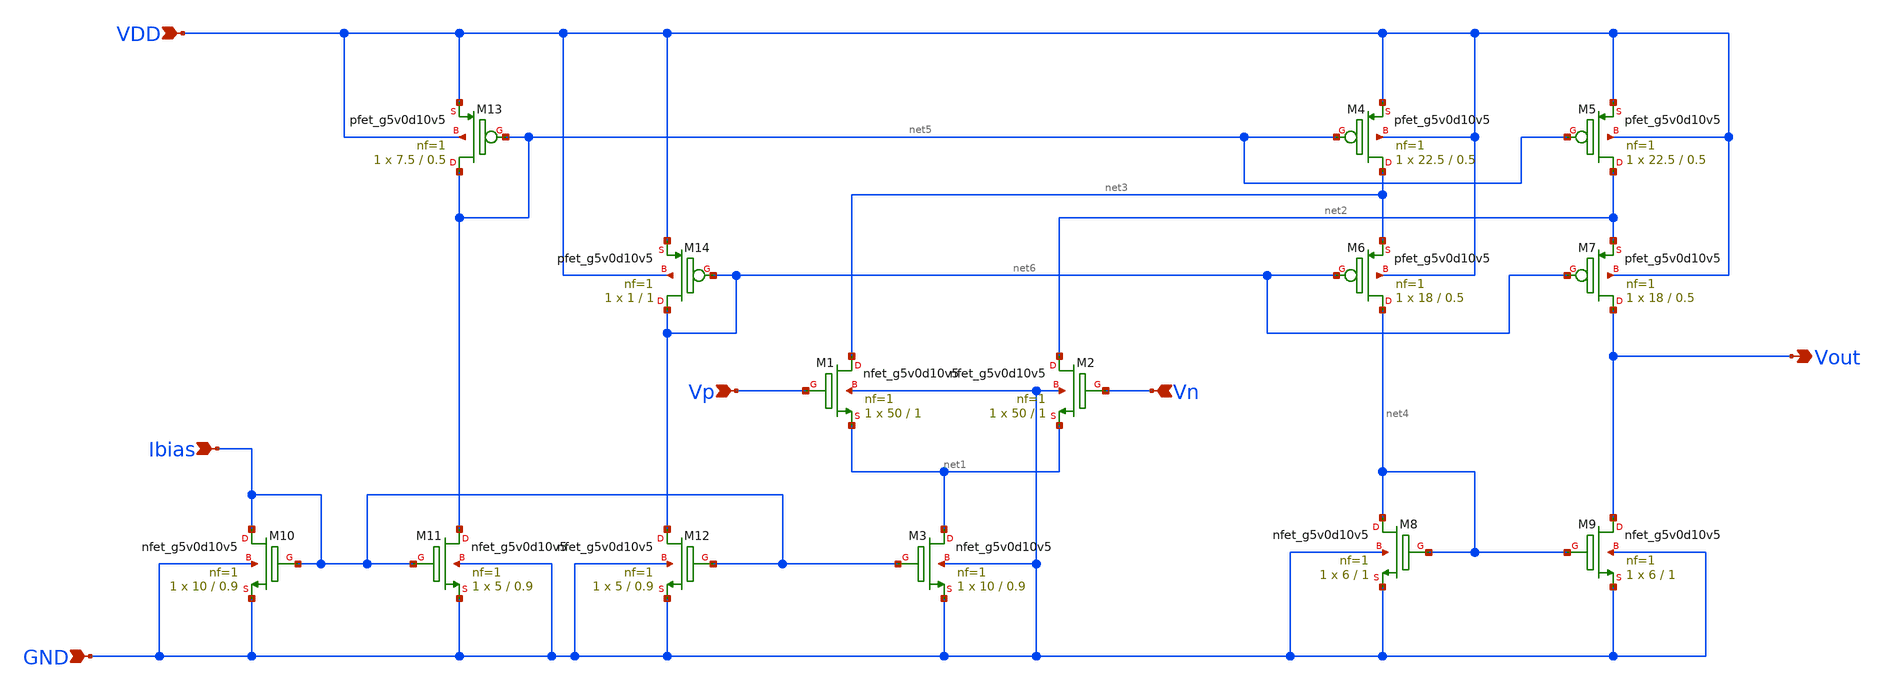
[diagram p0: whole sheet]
** sch_path: Analog_Blocks/OTA/Schematic/Folded_Cascode_OTA/Transitor5v/Folded_Cascode_OTA_5v.sch
**.subckt Folded_Cascode_OTA_5v VDD GND Vp Vn Vout Ibias
*.ipin VDD
*.ipin GND
*.ipin Vp
*.ipin Vn
*.opin Vout
*.ipin Ibias
XM1 net3 Vp net1 GND sky130_fd_pr__nfet_g5v0d10v5 L=1 W=50 nf=1 ad='int((nf+1)/2) * W/nf * 0.29' as='int((nf+2)/2) * W/nf * 0.29'
+ pd='2*int((nf+1)/2) * (W/nf + 0.29)' ps='2*int((nf+2)/2) * (W/nf + 0.29)' nrd='0.29 / W' nrs='0.29 / W'
+ sa=0 sb=0 sd=0 mult=1 m=1
XM2 net2 Vn net1 GND sky130_fd_pr__nfet_g5v0d10v5 L=1 W=50 nf=1 ad='int((nf+1)/2) * W/nf * 0.29' as='int((nf+2)/2) * W/nf * 0.29'
+ pd='2*int((nf+1)/2) * (W/nf + 0.29)' ps='2*int((nf+2)/2) * (W/nf + 0.29)' nrd='0.29 / W' nrs='0.29 / W'
+ sa=0 sb=0 sd=0 mult=1 m=1
XM9 Vout net4 GND GND sky130_fd_pr__nfet_g5v0d10v5 L=1 W=6 nf=1 ad='int((nf+1)/2) * W/nf * 0.29' as='int((nf+2)/2) * W/nf * 0.29'
+ pd='2*int((nf+1)/2) * (W/nf + 0.29)' ps='2*int((nf+2)/2) * (W/nf + 0.29)' nrd='0.29 / W' nrs='0.29 / W'
+ sa=0 sb=0 sd=0 mult=1 m=1
XM6 net4 net6 net3 VDD sky130_fd_pr__pfet_g5v0d10v5 L=0.5 W=18 nf=1 ad='int((nf+1)/2) * W/nf * 0.29'
+ as='int((nf+2)/2) * W/nf * 0.29' pd='2*int((nf+1)/2) * (W/nf + 0.29)' ps='2*int((nf+2)/2) * (W/nf + 0.29)'
+ nrd='0.29 / W' nrs='0.29 / W' sa=0 sb=0 sd=0 mult=1 m=1
XM5 net2 net5 VDD VDD sky130_fd_pr__pfet_g5v0d10v5 L=0.5 W=22.5 nf=1 ad='int((nf+1)/2) * W/nf * 0.29'
+ as='int((nf+2)/2) * W/nf * 0.29' pd='2*int((nf+1)/2) * (W/nf + 0.29)' ps='2*int((nf+2)/2) * (W/nf + 0.29)'
+ nrd='0.29 / W' nrs='0.29 / W' sa=0 sb=0 sd=0 mult=1 m=1
XM4 net3 net5 VDD VDD sky130_fd_pr__pfet_g5v0d10v5 L=0.5 W=22.5 nf=1 ad='int((nf+1)/2) * W/nf * 0.29'
+ as='int((nf+2)/2) * W/nf * 0.29' pd='2*int((nf+1)/2) * (W/nf + 0.29)' ps='2*int((nf+2)/2) * (W/nf + 0.29)'
+ nrd='0.29 / W' nrs='0.29 / W' sa=0 sb=0 sd=0 mult=1 m=1
XM3 net1 Ibias GND GND sky130_fd_pr__nfet_g5v0d10v5 L=0.9 W=10 nf=1 ad='int((nf+1)/2) * W/nf * 0.29'
+ as='int((nf+2)/2) * W/nf * 0.29' pd='2*int((nf+1)/2) * (W/nf + 0.29)' ps='2*int((nf+2)/2) * (W/nf + 0.29)'
+ nrd='0.29 / W' nrs='0.29 / W' sa=0 sb=0 sd=0 mult=1 m=1
XM7 Vout net6 net2 VDD sky130_fd_pr__pfet_g5v0d10v5 L=0.5 W=18 nf=1 ad='int((nf+1)/2) * W/nf * 0.29'
+ as='int((nf+2)/2) * W/nf * 0.29' pd='2*int((nf+1)/2) * (W/nf + 0.29)' ps='2*int((nf+2)/2) * (W/nf + 0.29)'
+ nrd='0.29 / W' nrs='0.29 / W' sa=0 sb=0 sd=0 mult=1 m=1
XM8 net4 net4 GND GND sky130_fd_pr__nfet_g5v0d10v5 L=1 W=6 nf=1 ad='int((nf+1)/2) * W/nf * 0.29' as='int((nf+2)/2) * W/nf * 0.29'
+ pd='2*int((nf+1)/2) * (W/nf + 0.29)' ps='2*int((nf+2)/2) * (W/nf + 0.29)' nrd='0.29 / W' nrs='0.29 / W'
+ sa=0 sb=0 sd=0 mult=1 m=1
XM10 Ibias Ibias GND GND sky130_fd_pr__nfet_g5v0d10v5 L=0.9 W=10 nf=1 ad='int((nf+1)/2) * W/nf * 0.29'
+ as='int((nf+2)/2) * W/nf * 0.29' pd='2*int((nf+1)/2) * (W/nf + 0.29)' ps='2*int((nf+2)/2) * (W/nf + 0.29)'
+ nrd='0.29 / W' nrs='0.29 / W' sa=0 sb=0 sd=0 mult=1 m=1
XM11 net5 Ibias GND GND sky130_fd_pr__nfet_g5v0d10v5 L=0.9 W=5 nf=1 ad='int((nf+1)/2) * W/nf * 0.29'
+ as='int((nf+2)/2) * W/nf * 0.29' pd='2*int((nf+1)/2) * (W/nf + 0.29)' ps='2*int((nf+2)/2) * (W/nf + 0.29)'
+ nrd='0.29 / W' nrs='0.29 / W' sa=0 sb=0 sd=0 mult=1 m=1
XM12 net6 Ibias GND GND sky130_fd_pr__nfet_g5v0d10v5 L=0.9 W=5 nf=1 ad='int((nf+1)/2) * W/nf * 0.29'
+ as='int((nf+2)/2) * W/nf * 0.29' pd='2*int((nf+1)/2) * (W/nf + 0.29)' ps='2*int((nf+2)/2) * (W/nf + 0.29)'
+ nrd='0.29 / W' nrs='0.29 / W' sa=0 sb=0 sd=0 mult=1 m=1
XM13 net5 net5 VDD VDD sky130_fd_pr__pfet_g5v0d10v5 L=0.5 W=7.5 nf=1 ad='int((nf+1)/2) * W/nf * 0.29'
+ as='int((nf+2)/2) * W/nf * 0.29' pd='2*int((nf+1)/2) * (W/nf + 0.29)' ps='2*int((nf+2)/2) * (W/nf + 0.29)'
+ nrd='0.29 / W' nrs='0.29 / W' sa=0 sb=0 sd=0 mult=1 m=1
XM14 net6 net6 VDD VDD sky130_fd_pr__pfet_g5v0d10v5 L=1 W=1 nf=1 ad='int((nf+1)/2) * W/nf * 0.29' as='int((nf+2)/2) * W/nf * 0.29'
+ pd='2*int((nf+1)/2) * (W/nf + 0.29)' ps='2*int((nf+2)/2) * (W/nf + 0.29)' nrd='0.29 / W' nrs='0.29 / W'
+ sa=0 sb=0 sd=0 mult=1 m=1
**.ends
.end
